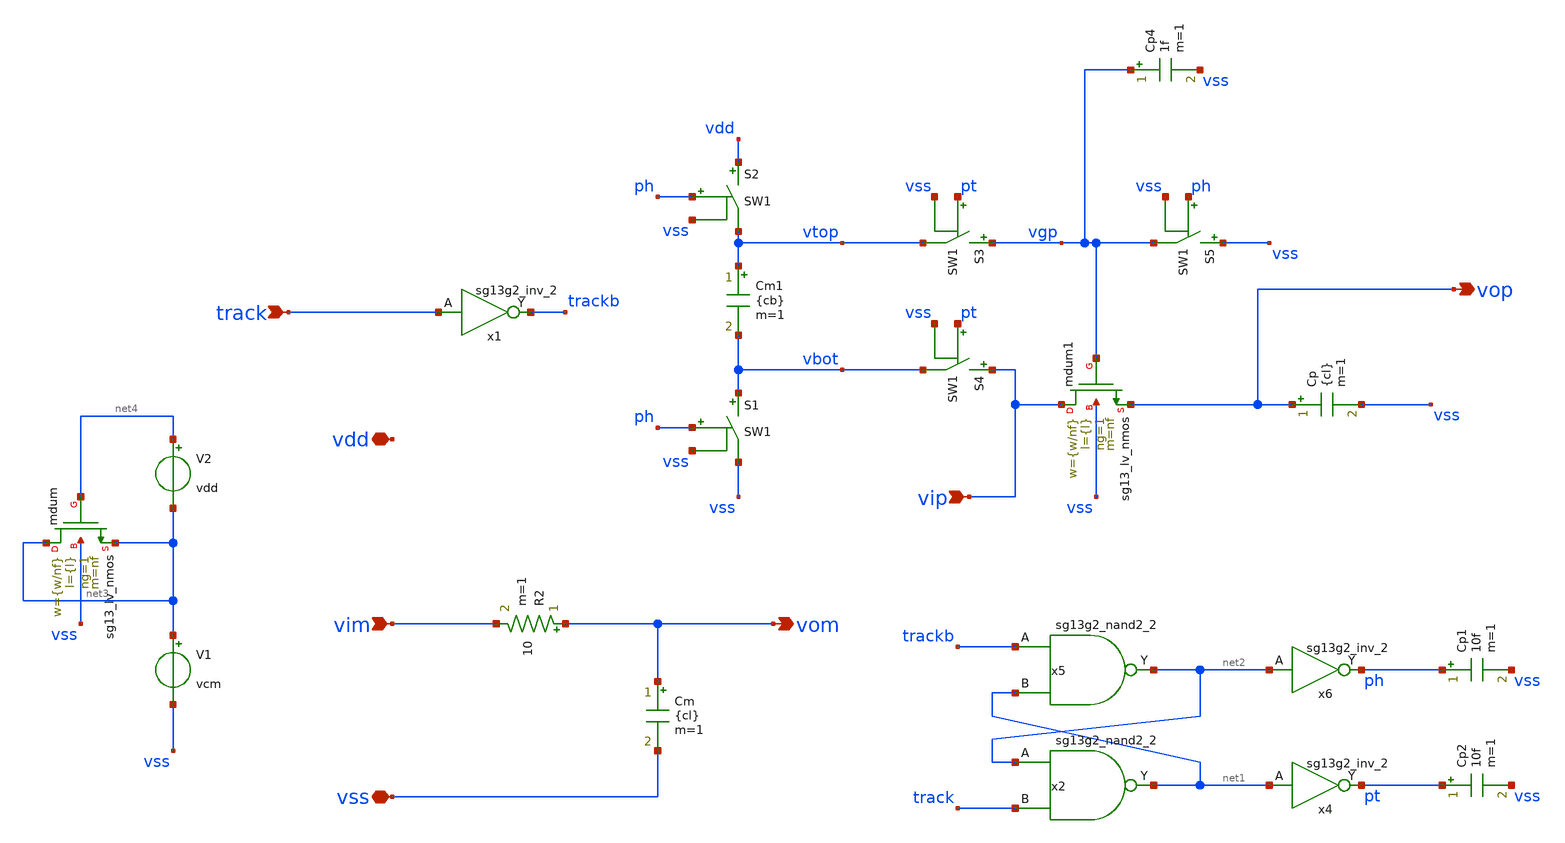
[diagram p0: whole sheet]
** sch_path: old/xschem/th_boot.sch
* IHP-GmbH/IHP-Open-PDK/ihp-sg13g2/libs.tech/xschem/sg13g2_stdcells/sg13g2_inv_2.sch:
* Copyright 2023 IHP PDK Authors
* Licensed under the Apache License, Version 2.0 (the "License");
**.subckt th_boot vip vim vom track vss vdd vop
*.ipin vip
*.ipin vim
*.opin vom
*.ipin track
*.iopin vss
*.iopin vdd
*.opin vop
Cm vom vss {cl} m=1
Cm1 vtop vbot {cb} m=1
S1 vbot vss ph vss SW1
S2 vdd vtop ph vss SW1
S3 vgp vtop pt vss SW1
S4 vip vbot pt vss SW1
S5 vss vgp ph vss SW1
V1 net3 vss vcm
V2 net4 net3 vdd
Cp1 ph vss 10f m=1
Cp2 pt vss 10f m=1
Cp vop vss {cl} m=1
x6 ph net2 VDD VSS sg13g2_inv_2
x4 pt net1 VDD VSS sg13g2_inv_2
x1 trackb track VDD VSS sg13g2_inv_2
x5 net2 trackb net1 VDD VSS sg13g2_nand2_2
x2 net1 net2 track VDD VSS sg13g2_nand2_2
Xmdum net3 net4 net3 vss sg13_lv_nmos w={w/nf} l={l} ng=1 m=nf mm_ok=1
Cp4 vgp vss 1f m=1
R2 vom vim 10 m=1
Xmdum1 vip vgp vop vss sg13_lv_nmos w={w/nf} l={l} ng=1 m=nf mm_ok=1
**.ends

* expanding   symbol:  sg13g2_inv_2.sym # of pins=2
** sym_path: sg13g2_inv_2.sym
** sch_path: sg13g2_inv_2.sch
.subckt sg13g2_inv_2 Y A VDD VSS
*.opin Y
*.ipin A
*.iopin VDD
*.iopin VSS
XM1 Y A VSS VSS sg13_lv_nmos w=1.48u l=130.00n ng=2 m=1 mm_ok=1
XM2 Y A VDD VDD sg13_lv_pmos w=2.24u l=130.00n ng=2 m=1 mm_ok=1
.ends


* expanding   symbol:  sg13g2_nand2_2.sym # of pins=3
** sym_path: sg13g2_nand2_2.sym
** sch_path: sg13g2_nand2_2.sch
.subckt sg13g2_nand2_2 Y A B VDD VSS
*.iopin VDD
*.iopin VSS
*.opin Y
*.ipin B
*.ipin A
XM1 Y A net1 VSS sg13_lv_nmos w=1.44u l=130.00n ng=2 m=1 mm_ok=1
XM2 net1 B VSS VSS sg13_lv_nmos w=1.44u l=130.00n ng=2 m=1 mm_ok=1
XM3 Y A VDD VDD sg13_lv_pmos w=2.24u l=130.00n ng=2 m=1 mm_ok=1
XM4 Y B VDD VDD sg13_lv_pmos w=2.24u l=130.00n ng=2 m=1 mm_ok=1
.ends

**** begin user architecture code
.MODEL SW1 SW   VT=0.6 VH=vh  RON=1 ROFF=roff
**** end user architecture code
.end
